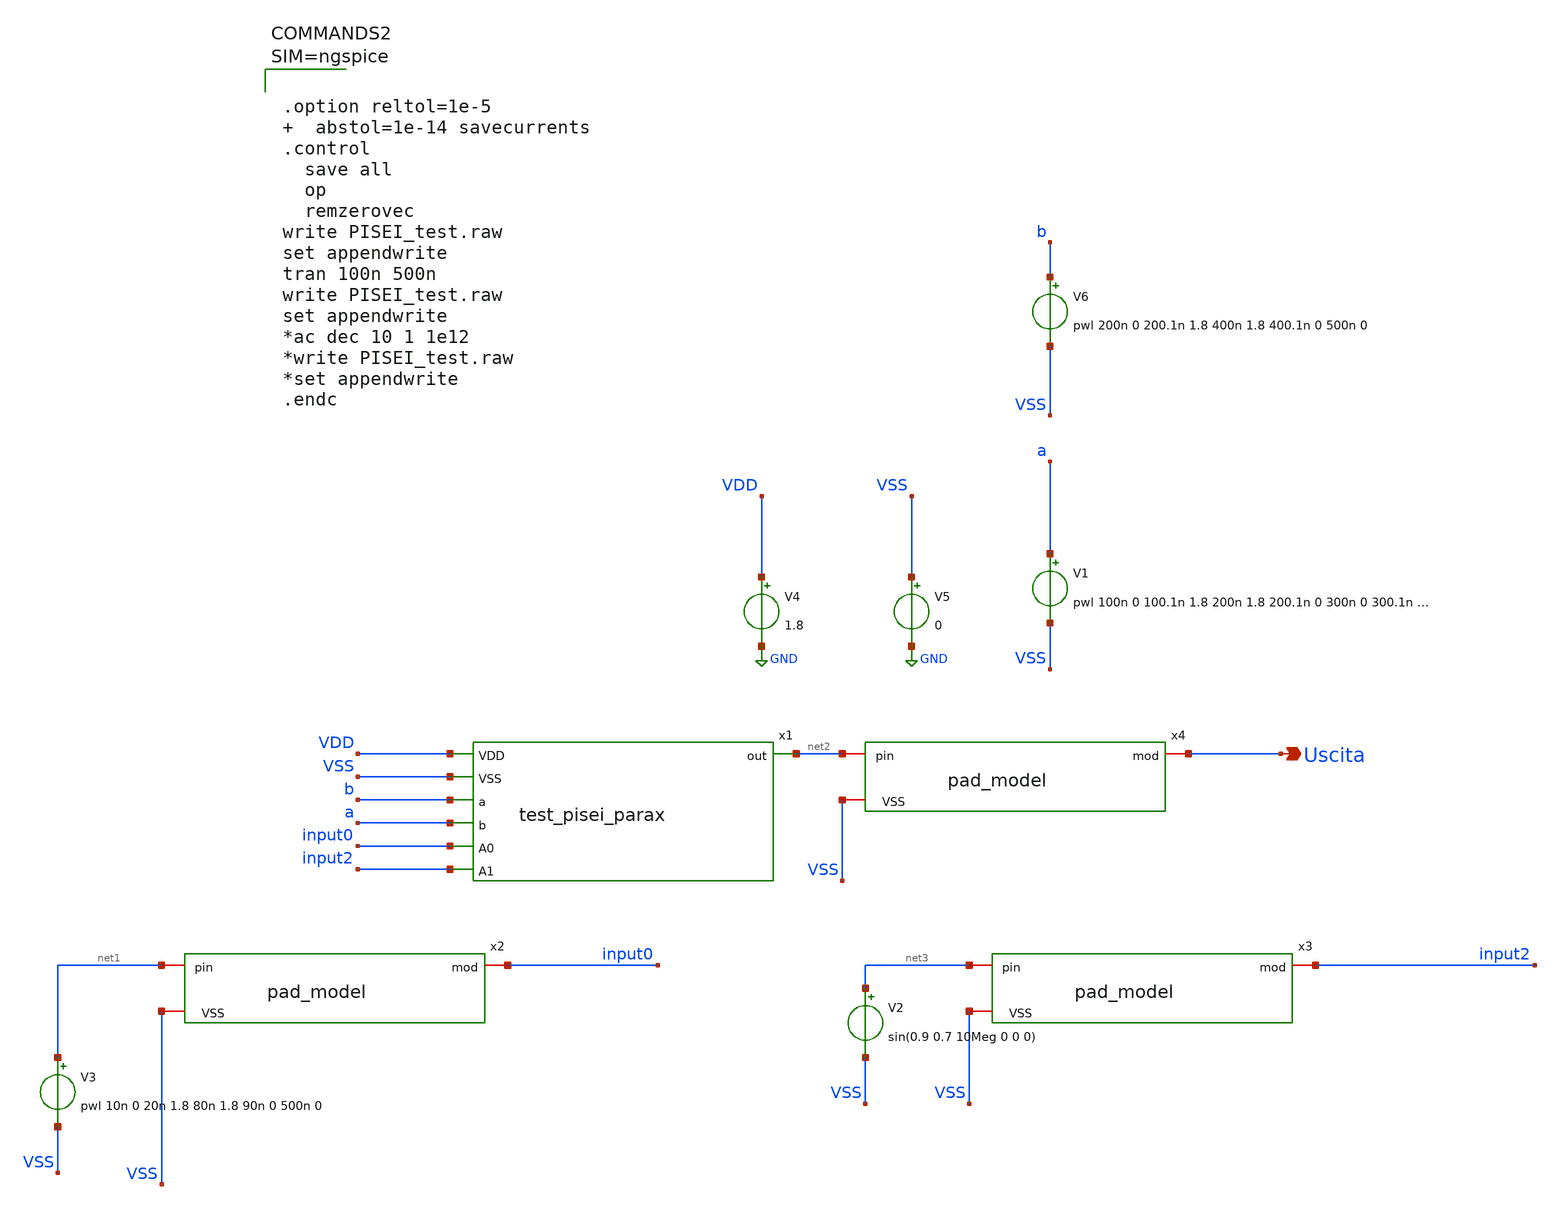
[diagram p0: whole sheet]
** sch_path: xschem/PISEI_test.sch
**.subckt PISEI_test Uscita
*.opin Uscita
V4 VDD GND 1.8
V5 VSS GND 0
V2 net3 VSS sin(0.9 0.7 10Meg 0 0 0)
V3 net1 VSS pwl 10n 0 20n 1.8 80n 1.8 90n 0 500n 0
V1 a VSS pwl 100n 0 100.1n 1.8 200n 1.8 200.1n 0 300n 0 300.1n 1.8 400n 1.8 400.1n 0 500n 0
V6 b VSS pwl 200n 0 200.1n 1.8 400n 1.8 400.1n 0 500n 0
x2 VSS net1 input0 pad_model
x3 VSS net3 input2 pad_model
x4 VSS net2 Uscita pad_model
x1 VDD VSS net2 b a input0 input2 test_pisei_parax
**** begin user architecture code



.option reltol=1e-5   abstol=1e-14 savecurrents
.control
  save all
  op
  remzerovec
write PISEI_test.raw
set appendwrite
tran 100n 500n
write PISEI_test.raw
set appendwrite
*ac dec 10 1 1e12
*write PISEI_test.raw
*set appendwrite
.endc




** opencircuitdesign pdks install
.lib $::SKYWATER_MODELS/sky130.lib.spice tt


**** end user architecture code
**.ends
.GLOBAL GND
.end
